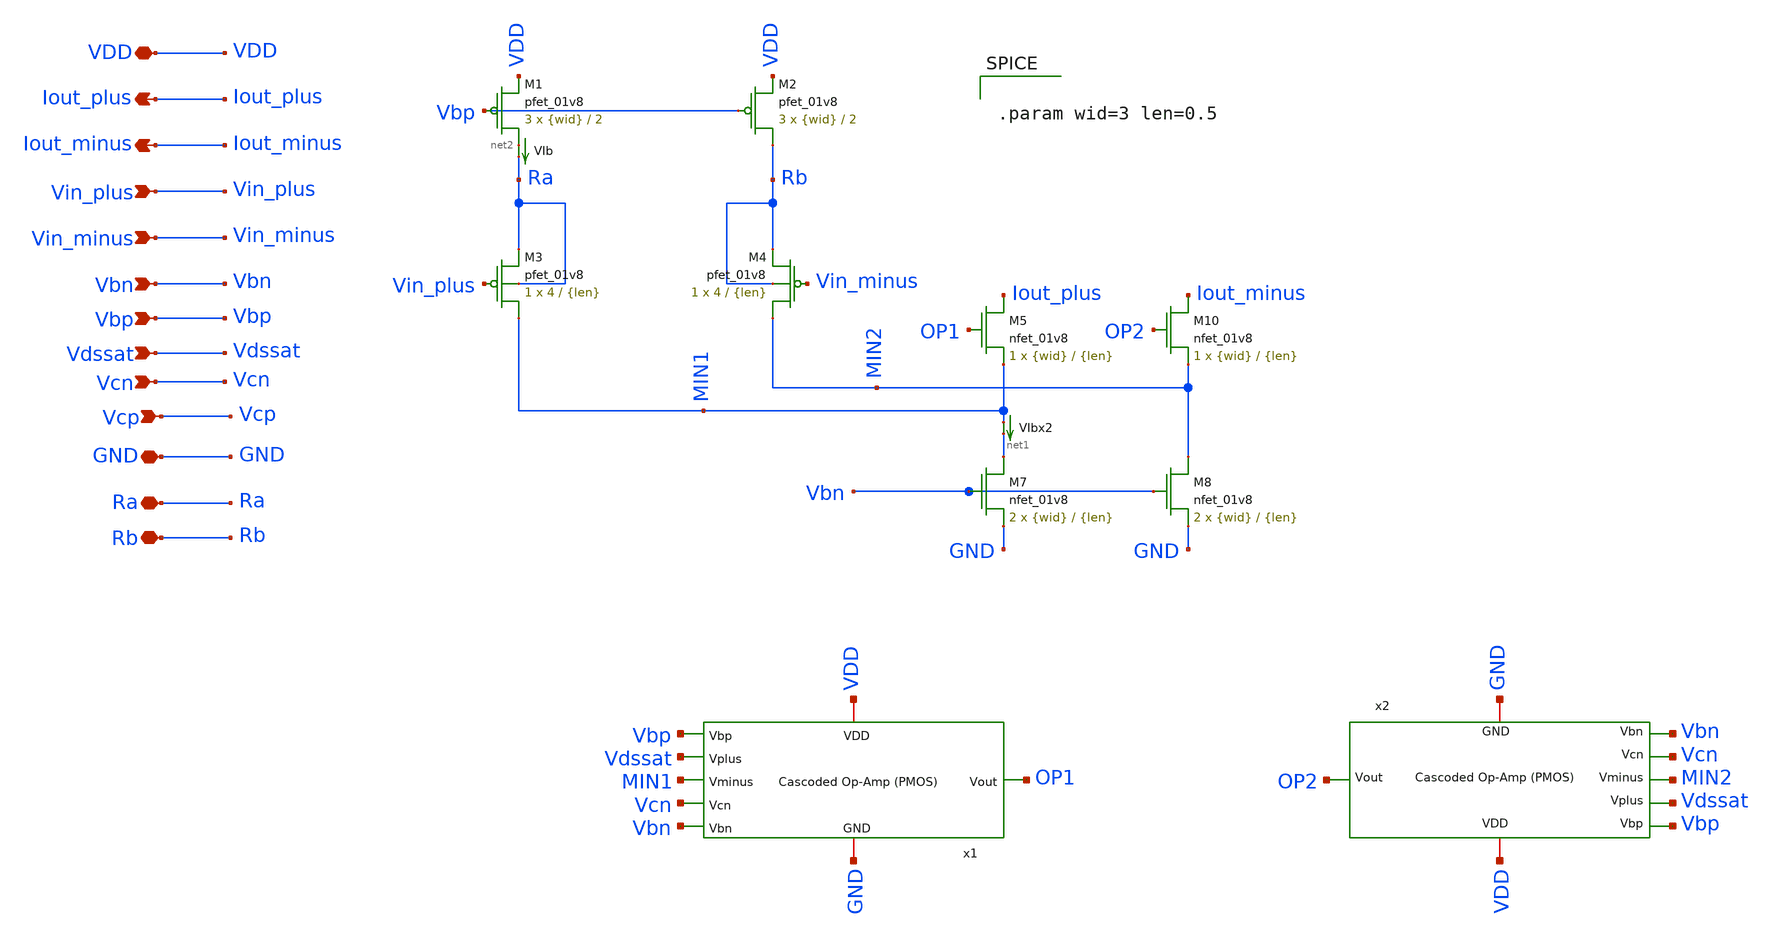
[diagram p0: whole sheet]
** sch_path: final/schematics/brad_VI_input.sch
**.subckt brad_VI_input Iout_plus Iout_minus VDD Vin_plus Vin_minus Vbn GND Ra Rb Vbp Vdssat Vcn Vcp
*.opin Iout_plus
*.opin Iout_minus
*.iopin VDD
*.ipin Vin_plus
*.ipin Vin_minus
*.ipin Vbn
*.iopin GND
*.iopin Ra
*.iopin Rb
*.ipin Vbp
*.ipin Vdssat
*.ipin Vcn
*.ipin Vcp
XM3 MIN1 Vin_plus Ra Ra sky130_fd_pr__pfet_01v8 L={len} W=4 nf=1 ad='int((nf+1)/2) * W/nf * 0.29' as='int((nf+2)/2) * W/nf * 0.29'
+ pd='2*int((nf+1)/2) * (W/nf + 0.29)' ps='2*int((nf+2)/2) * (W/nf + 0.29)' nrd='0.29 / W' nrs='0.29 / W'
+ sa=0 sb=0 sd=0 mult=1 m=1
XM5 Iout_plus OP1 MIN1 GND sky130_fd_pr__nfet_01v8 L={len} W={wid} nf=1 ad='int((nf+1)/2) * W/nf * 0.29'
+ as='int((nf+2)/2) * W/nf * 0.29' pd='2*int((nf+1)/2) * (W/nf + 0.29)' ps='2*int((nf+2)/2) * (W/nf + 0.29)'
+ nrd='0.29 / W' nrs='0.29 / W' sa=0 sb=0 sd=0 mult=1 m=1
VIb net2 Ra 0
.save i(vib)
XM4 MIN2 Vin_minus Rb Rb sky130_fd_pr__pfet_01v8 L={len} W=4 nf=1 ad='int((nf+1)/2) * W/nf * 0.29' as='int((nf+2)/2) * W/nf * 0.29'
+ pd='2*int((nf+1)/2) * (W/nf + 0.29)' ps='2*int((nf+2)/2) * (W/nf + 0.29)' nrd='0.29 / W' nrs='0.29 / W'
+ sa=0 sb=0 sd=0 mult=1 m=1
XM7 net1 Vbn GND GND sky130_fd_pr__nfet_01v8 L={len} W={wid} nf=1 ad='int((nf+1)/2) * W/nf * 0.29' as='int((nf+2)/2) * W/nf * 0.29'
+ pd='2*int((nf+1)/2) * (W/nf + 0.29)' ps='2*int((nf+2)/2) * (W/nf + 0.29)' nrd='0.29 / W' nrs='0.29 / W'
+ sa=0 sb=0 sd=0 mult=2 m=2
XM8 MIN2 Vbn GND GND sky130_fd_pr__nfet_01v8 L={len} W={wid} nf=1 ad='int((nf+1)/2) * W/nf * 0.29' as='int((nf+2)/2) * W/nf * 0.29'
+ pd='2*int((nf+1)/2) * (W/nf + 0.29)' ps='2*int((nf+2)/2) * (W/nf + 0.29)' nrd='0.29 / W' nrs='0.29 / W'
+ sa=0 sb=0 sd=0 mult=2 m=2
XM10 Iout_minus OP2 MIN2 GND sky130_fd_pr__nfet_01v8 L={len} W={wid} nf=1 ad='int((nf+1)/2) * W/nf * 0.29'
+ as='int((nf+2)/2) * W/nf * 0.29' pd='2*int((nf+1)/2) * (W/nf + 0.29)' ps='2*int((nf+2)/2) * (W/nf + 0.29)'
+ nrd='0.29 / W' nrs='0.29 / W' sa=0 sb=0 sd=0 mult=1 m=1
VIbx2 MIN1 net1 0
.save i(vibx2)
x1 Vbp Vdssat MIN1 Vcn Vbn VDD GND OP1 cascoded_opamp_pmos
x2 Vbp Vdssat MIN2 Vcn Vbn VDD GND OP2 cascoded_opamp_pmos
XM1 net2 Vbp VDD VDD sky130_fd_pr__pfet_01v8 L=2 W={wid} nf=1 ad='int((nf+1)/2) * W/nf * 0.29' as='int((nf+2)/2) * W/nf * 0.29'
+ pd='2*int((nf+1)/2) * (W/nf + 0.29)' ps='2*int((nf+2)/2) * (W/nf + 0.29)' nrd='0.29 / W' nrs='0.29 / W'
+ sa=0 sb=0 sd=0 mult=3 m=3
XM2 Rb Vbp VDD VDD sky130_fd_pr__pfet_01v8 L=2 W={wid} nf=1 ad='int((nf+1)/2) * W/nf * 0.29' as='int((nf+2)/2) * W/nf * 0.29'
+ pd='2*int((nf+1)/2) * (W/nf + 0.29)' ps='2*int((nf+2)/2) * (W/nf + 0.29)' nrd='0.29 / W' nrs='0.29 / W'
+ sa=0 sb=0 sd=0 mult=3 m=3
**** begin user architecture code


.param wid=3 len=0.5


**** end user architecture code
**.ends
.end
